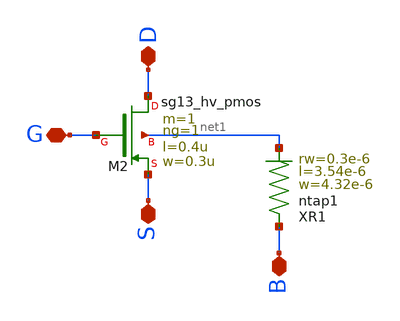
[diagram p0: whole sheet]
** sch_path: ihp-sg13cmos5l/schematic/xschem/sg13_hv_pmos_ring_pcell.sch
**.subckt sg13_hv_pmos_ring_pcell D S G B
*.iopin D
*.iopin S
*.iopin G
*.iopin B
XM2 D G S net1 sg13_hv_pmos w=0.3u l=0.4u ng=1 m=1 mm_ok=1
XR1 B net1 ntap1 R=15.7 w=4.32e-6 l=3.54e-6 rw=0.3e-6
**.ends
.end
